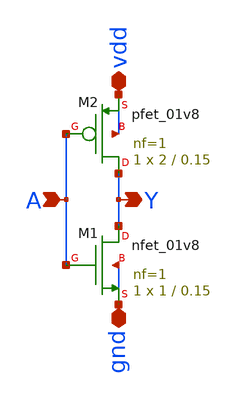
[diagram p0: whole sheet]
** sch_path: Circuit Files/circuits/first_test/inverter_check.sch
**.subckt inverter_check A Y vdd gnd
*.ipin A
*.opin Y
*.iopin vdd
*.iopin gnd
XM2 Y A vdd vdd sky130_fd_pr__pfet_01v8 L=0.15 W=2 nf=1 ad='int((nf+1)/2) * W/nf * 0.29' as='int((nf+2)/2) * W/nf * 0.29'
+ pd='2*int((nf+1)/2) * (W/nf + 0.29)' ps='2*int((nf+2)/2) * (W/nf + 0.29)' nrd='0.29 / W' nrs='0.29 / W'
+ sa=0 sb=0 sd=0 mult=1 m=1
XM1 Y A gnd gnd sky130_fd_pr__nfet_01v8 L=0.15 W=1 nf=1 ad='int((nf+1)/2) * W/nf * 0.29' as='int((nf+2)/2) * W/nf * 0.29'
+ pd='2*int((nf+1)/2) * (W/nf + 0.29)' ps='2*int((nf+2)/2) * (W/nf + 0.29)' nrd='0.29 / W' nrs='0.29 / W'
+ sa=0 sb=0 sd=0 mult=1 m=1
**.ends
.end
